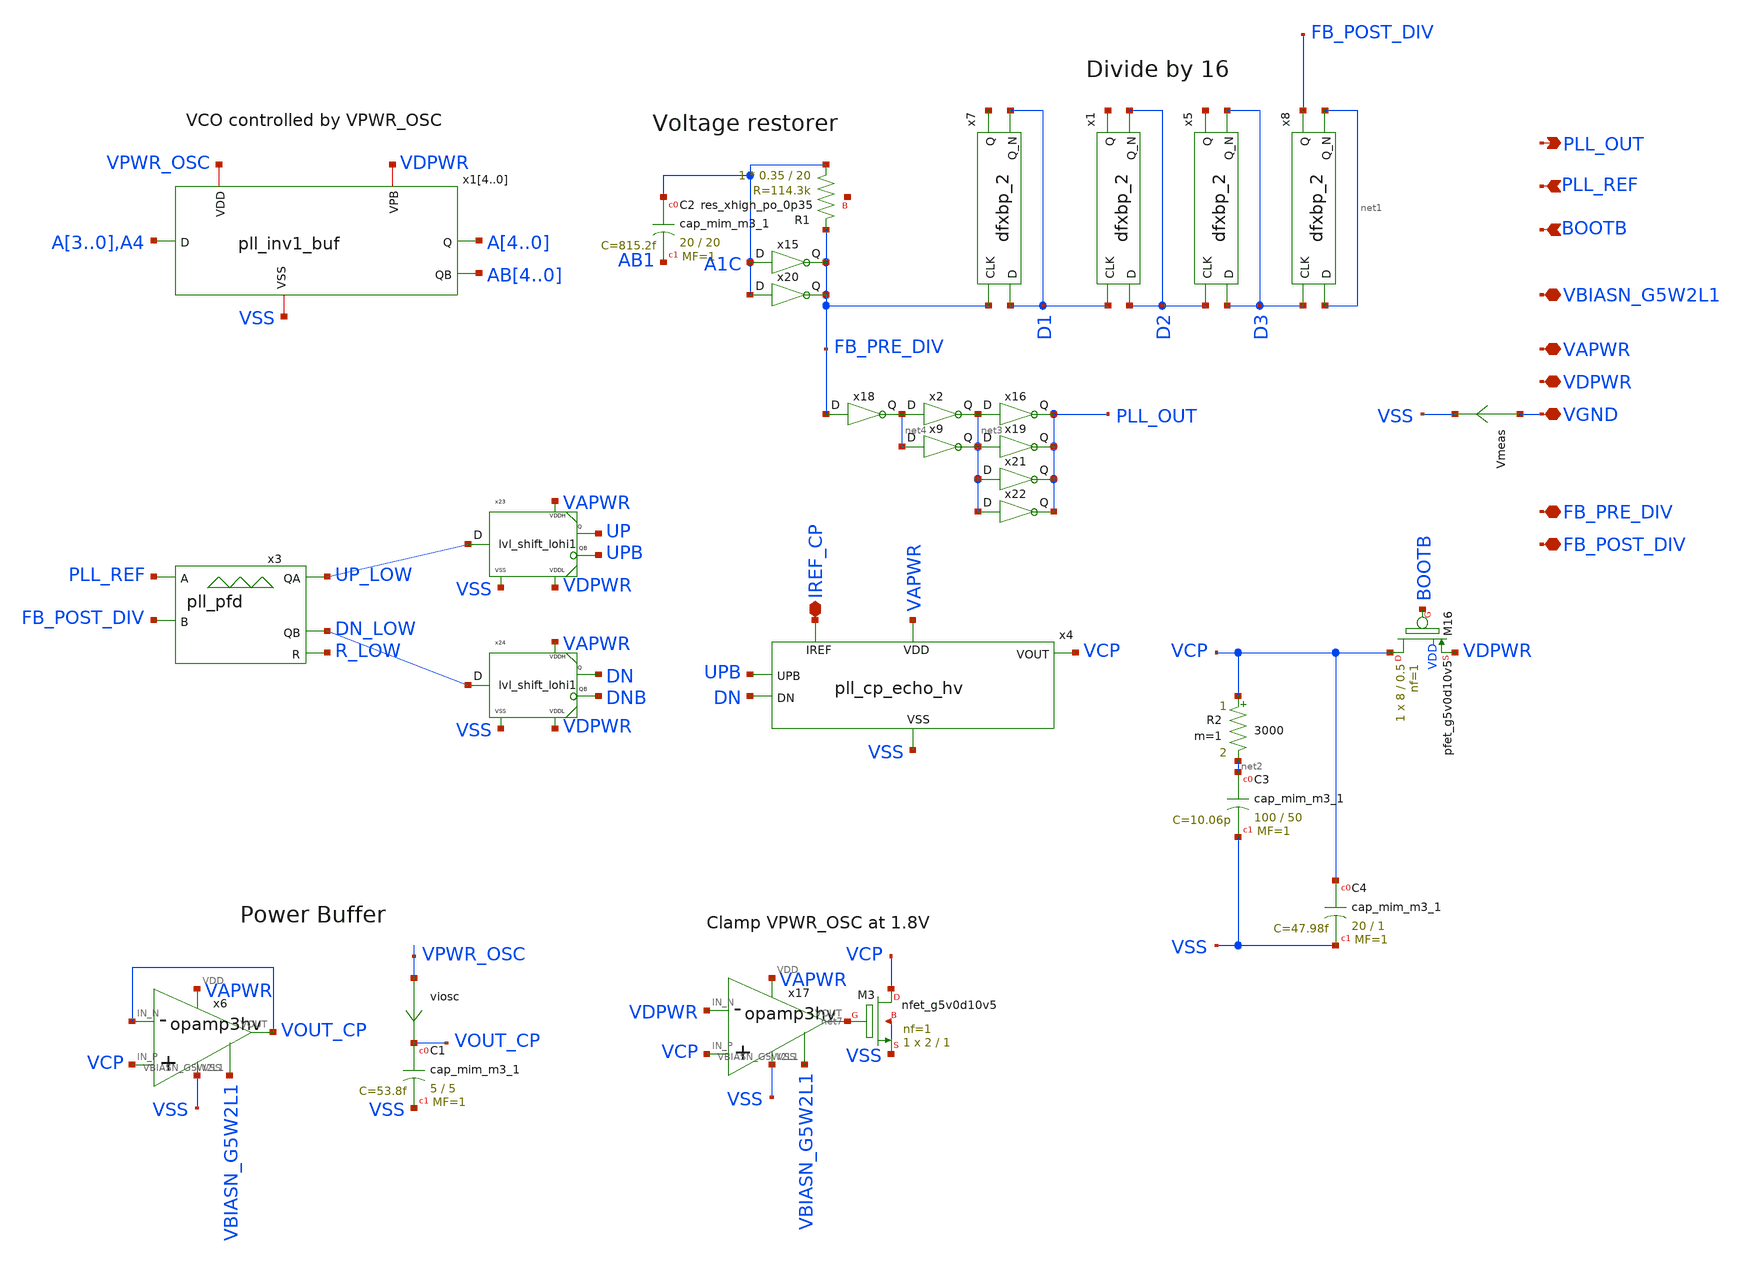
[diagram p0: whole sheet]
** sch_path: xschem/tt08_pll.sch
**.subckt tt08_pll IREF_CP VDPWR VGND VAPWR PLL_OUT PLL_REF BOOTB VBIASN_G5W2L1 FB_PRE_DIV
*+ FB_POST_DIV
*.iopin IREF_CP
*.iopin VDPWR
*.iopin VGND
*.iopin VAPWR
*.opin PLL_OUT
*.ipin PLL_REF
*.ipin BOOTB
*.iopin VBIASN_G5W2L1
*.iopin FB_PRE_DIV
*.iopin FB_POST_DIV
x3 PLL_REF FB_POST_DIV UP_LOW DN_LOW R_LOW VDPWR VSS pll_pfd
x7 FB_PRE_DIV D1 VGND VGND VDPWR VDPWR net5 D1 sky130_fd_sc_hd__dfxbp_2
x15 A1C FB_PRE_DIV VDPWR VSS pll_inv1
XR1 A1C FB_PRE_DIV net6 sky130_fd_pr__res_xhigh_po_0p35 L=20 mult=1 m=1
XC2 A1C AB1 sky130_fd_pr__cap_mim_m3_1 W=20 L=20 MF=1 m=1
viosc VPWR_OSC VOUT_CP 0
.save i(viosc)
x6 VOUT_CP VCP VOUT_CP VBIASN_G5W2L1 VAPWR VSS opamp3hv
x23 UP_LOW UP UPB VAPWR VDPWR VSS lvl_shift_lohi1
x24 DN_LOW DN DNB VAPWR VDPWR VSS lvl_shift_lohi1
XC1 VOUT_CP VSS sky130_fd_pr__cap_mim_m3_1 W=5 L=5 MF=1 m=1
x14 A3 A4 AB4 VDPWR VPWR_OSC VSS pll_inv1_buf
x13 A2 A3 AB3 VDPWR VPWR_OSC VSS pll_inv1_buf
x12 A1 A2 AB2 VDPWR VPWR_OSC VSS pll_inv1_buf
x11 A0 A1 AB1 VDPWR VPWR_OSC VSS pll_inv1_buf
x10 A4 A0 AB0 VDPWR VPWR_OSC VSS pll_inv1_buf
x20 A1C FB_PRE_DIV VDPWR VSS pll_inv1
x4 UPB DN VCP IREF_CP VAPWR VSS pll_cp_echo_hv
XC3 net2 VSS sky130_fd_pr__cap_mim_m3_1 W=100 L=50 MF=1 m=1
R2 VCP net2 3000 m=1
XC4 VCP VSS sky130_fd_pr__cap_mim_m3_1 W=20 L=1 MF=1 m=1
XM16 VCP BOOTB VDPWR VDD sky130_fd_pr__pfet_g5v0d10v5 L=0.5 W=8 nf=1 ad='int((nf+1)/2) * W/nf * 0.29'
+ as='int((nf+2)/2) * W/nf * 0.29' pd='2*int((nf+1)/2) * (W/nf + 0.29)' ps='2*int((nf+2)/2) * (W/nf + 0.29)'
+ nrd='0.29 / W' nrs='0.29 / W' sa=0 sb=0 sd=0 mult=1 m=1
x17 VDPWR VCP net7 VBIASN_G5W2L1 VAPWR VSS opamp3hv
XM3 VCP net7 VSS VSS sky130_fd_pr__nfet_g5v0d10v5 L=1 W=2 nf=1 ad='int((nf+1)/2) * W/nf * 0.29' as='int((nf+2)/2) * W/nf * 0.29'
+ pd='2*int((nf+1)/2) * (W/nf + 0.29)' ps='2*int((nf+2)/2) * (W/nf + 0.29)' nrd='0.29 / W' nrs='0.29 / W'
+ sa=0 sb=0 sd=0 mult=1 m=1
x1 D1 D2 VGND VGND VDPWR VDPWR net8 D2 sky130_fd_sc_hd__dfxbp_2
x5 D2 D3 VGND VGND VDPWR VDPWR net9 D3 sky130_fd_sc_hd__dfxbp_2
x8 D3 net1 VGND VGND VDPWR VDPWR FB_POST_DIV net1 sky130_fd_sc_hd__dfxbp_2
x18 FB_PRE_DIV net4 VDPWR VSS pll_inv1
x2 net4 net3 VDPWR VSS pll_inv1
x9 net4 net3 VDPWR VSS pll_inv1
x16 net3 PLL_OUT VDPWR VSS pll_inv1
x19 net3 PLL_OUT VDPWR VSS pll_inv1
x21 net3 PLL_OUT VDPWR VSS pll_inv1
x22 net3 PLL_OUT VDPWR VSS pll_inv1
Vmeas VGND VSS 0
.save i(vmeas)
**.ends
.end
